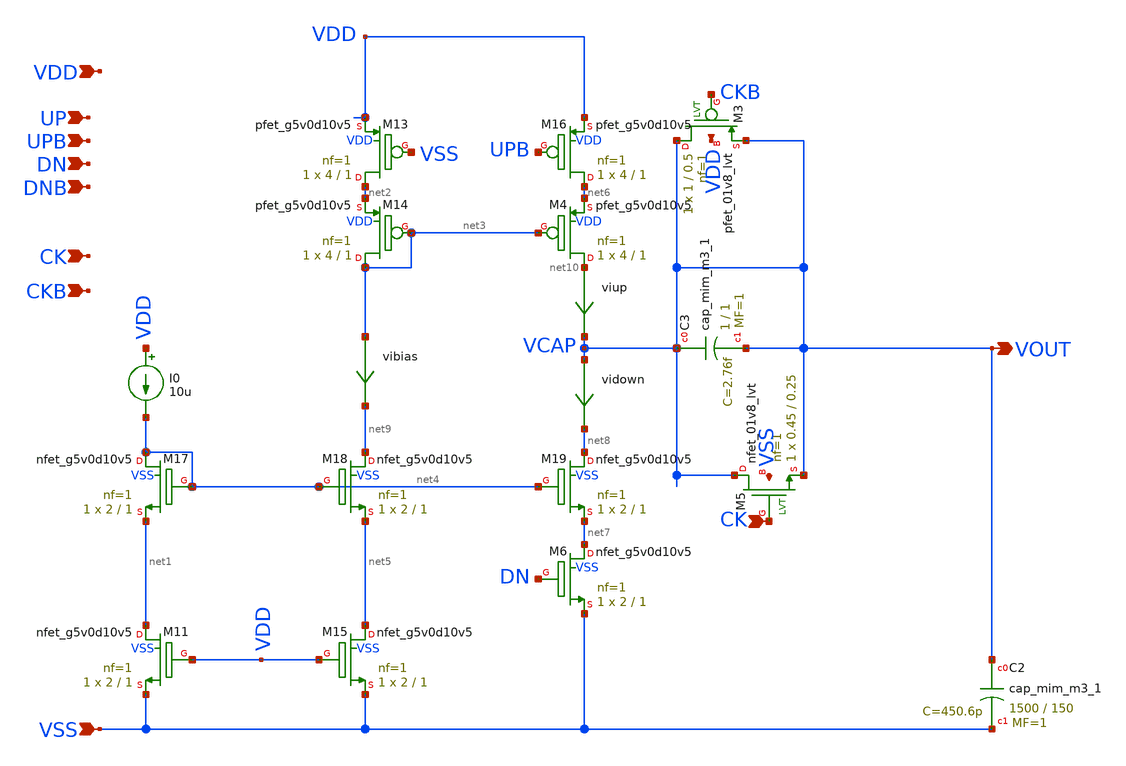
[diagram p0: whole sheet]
** sch_path: xschem/pll_cp_delta_hv.sch
**.subckt pll_cp_delta_hv VOUT VSS UP DNB CK CKB VDD DN UPB CK
*.opin VOUT
*.ipin VSS
*.ipin UP
*.ipin DNB
*.ipin CK
*.ipin CKB
*.ipin VDD
*.ipin DN
*.ipin UPB
*.ipin CK
vibias net3 net9 0
.save i(vibias)
XM16 net6 UPB VDD VDD sky130_fd_pr__pfet_g5v0d10v5 L=1 W=4 nf=1 ad='int((nf+1)/2) * W/nf * 0.29' as='int((nf+2)/2) * W/nf * 0.29'
+ pd='2*int((nf+1)/2) * (W/nf + 0.29)' ps='2*int((nf+2)/2) * (W/nf + 0.29)' nrd='0.29 / W' nrs='0.29 / W'
+ sa=0 sb=0 sd=0 mult=1 m=1
XM13 net2 VSS VDD VDD sky130_fd_pr__pfet_g5v0d10v5 L=1 W=4 nf=1 ad='int((nf+1)/2) * W/nf * 0.29' as='int((nf+2)/2) * W/nf * 0.29'
+ pd='2*int((nf+1)/2) * (W/nf + 0.29)' ps='2*int((nf+2)/2) * (W/nf + 0.29)' nrd='0.29 / W' nrs='0.29 / W'
+ sa=0 sb=0 sd=0 mult=1 m=1
XM14 net3 net3 net2 VDD sky130_fd_pr__pfet_g5v0d10v5 L=1 W=4 nf=1 ad='int((nf+1)/2) * W/nf * 0.29' as='int((nf+2)/2) * W/nf * 0.29'
+ pd='2*int((nf+1)/2) * (W/nf + 0.29)' ps='2*int((nf+2)/2) * (W/nf + 0.29)' nrd='0.29 / W' nrs='0.29 / W'
+ sa=0 sb=0 sd=0 mult=1 m=1
I0 VDD net4 10u
XM11 net1 VDD VSS VSS sky130_fd_pr__nfet_g5v0d10v5 L=1 W=2 nf=1 ad='int((nf+1)/2) * W/nf * 0.29' as='int((nf+2)/2) * W/nf * 0.29'
+ pd='2*int((nf+1)/2) * (W/nf + 0.29)' ps='2*int((nf+2)/2) * (W/nf + 0.29)' nrd='0.29 / W' nrs='0.29 / W'
+ sa=0 sb=0 sd=0 mult=1 m=1
XM17 net4 net4 net1 VSS sky130_fd_pr__nfet_g5v0d10v5 L=1 W=2 nf=1 ad='int((nf+1)/2) * W/nf * 0.29' as='int((nf+2)/2) * W/nf * 0.29'
+ pd='2*int((nf+1)/2) * (W/nf + 0.29)' ps='2*int((nf+2)/2) * (W/nf + 0.29)' nrd='0.29 / W' nrs='0.29 / W'
+ sa=0 sb=0 sd=0 mult=1 m=1
XM15 net5 VDD VSS VSS sky130_fd_pr__nfet_g5v0d10v5 L=1 W=2 nf=1 ad='int((nf+1)/2) * W/nf * 0.29' as='int((nf+2)/2) * W/nf * 0.29'
+ pd='2*int((nf+1)/2) * (W/nf + 0.29)' ps='2*int((nf+2)/2) * (W/nf + 0.29)' nrd='0.29 / W' nrs='0.29 / W'
+ sa=0 sb=0 sd=0 mult=1 m=1
XM18 net9 net4 net5 VSS sky130_fd_pr__nfet_g5v0d10v5 L=1 W=2 nf=1 ad='int((nf+1)/2) * W/nf * 0.29' as='int((nf+2)/2) * W/nf * 0.29'
+ pd='2*int((nf+1)/2) * (W/nf + 0.29)' ps='2*int((nf+2)/2) * (W/nf + 0.29)' nrd='0.29 / W' nrs='0.29 / W'
+ sa=0 sb=0 sd=0 mult=1 m=1
XM6 net7 DN VSS VSS sky130_fd_pr__nfet_g5v0d10v5 L=1 W=2 nf=1 ad='int((nf+1)/2) * W/nf * 0.29' as='int((nf+2)/2) * W/nf * 0.29'
+ pd='2*int((nf+1)/2) * (W/nf + 0.29)' ps='2*int((nf+2)/2) * (W/nf + 0.29)' nrd='0.29 / W' nrs='0.29 / W'
+ sa=0 sb=0 sd=0 mult=1 m=1
XM19 net8 net4 net7 VSS sky130_fd_pr__nfet_g5v0d10v5 L=1 W=2 nf=1 ad='int((nf+1)/2) * W/nf * 0.29' as='int((nf+2)/2) * W/nf * 0.29'
+ pd='2*int((nf+1)/2) * (W/nf + 0.29)' ps='2*int((nf+2)/2) * (W/nf + 0.29)' nrd='0.29 / W' nrs='0.29 / W'
+ sa=0 sb=0 sd=0 mult=1 m=1
XM4 net10 net3 net6 VDD sky130_fd_pr__pfet_g5v0d10v5 L=1 W=4 nf=1 ad='int((nf+1)/2) * W/nf * 0.29' as='int((nf+2)/2) * W/nf * 0.29'
+ pd='2*int((nf+1)/2) * (W/nf + 0.29)' ps='2*int((nf+2)/2) * (W/nf + 0.29)' nrd='0.29 / W' nrs='0.29 / W'
+ sa=0 sb=0 sd=0 mult=1 m=1
viup net10 VOUT 0
.save i(viup)
vidown VOUT net8 0
.save i(vidown)
XC3 VOUT VOUT sky130_fd_pr__cap_mim_m3_1 W=1 L=1 MF=1 m=1
XM3 VOUT CKB VOUT VDD sky130_fd_pr__pfet_01v8_lvt L=0.5 W=1 nf=1 ad='int((nf+1)/2) * W/nf * 0.29' as='int((nf+2)/2) * W/nf * 0.29'
+ pd='2*int((nf+1)/2) * (W/nf + 0.29)' ps='2*int((nf+2)/2) * (W/nf + 0.29)' nrd='0.29 / W' nrs='0.29 / W'
+ sa=0 sb=0 sd=0 mult=1 m=1
XM5 VOUT CK VOUT VSS sky130_fd_pr__nfet_01v8_lvt L=0.25 W=0.45 nf=1 ad='int((nf+1)/2) * W/nf * 0.29'
+ as='int((nf+2)/2) * W/nf * 0.29' pd='2*int((nf+1)/2) * (W/nf + 0.29)' ps='2*int((nf+2)/2) * (W/nf + 0.29)'
+ nrd='0.29 / W' nrs='0.29 / W' sa=0 sb=0 sd=0 mult=1 m=1
XC2 VOUT VSS sky130_fd_pr__cap_mim_m3_1 W=1500 L=150 MF=1 m=1
**.ends
.end
